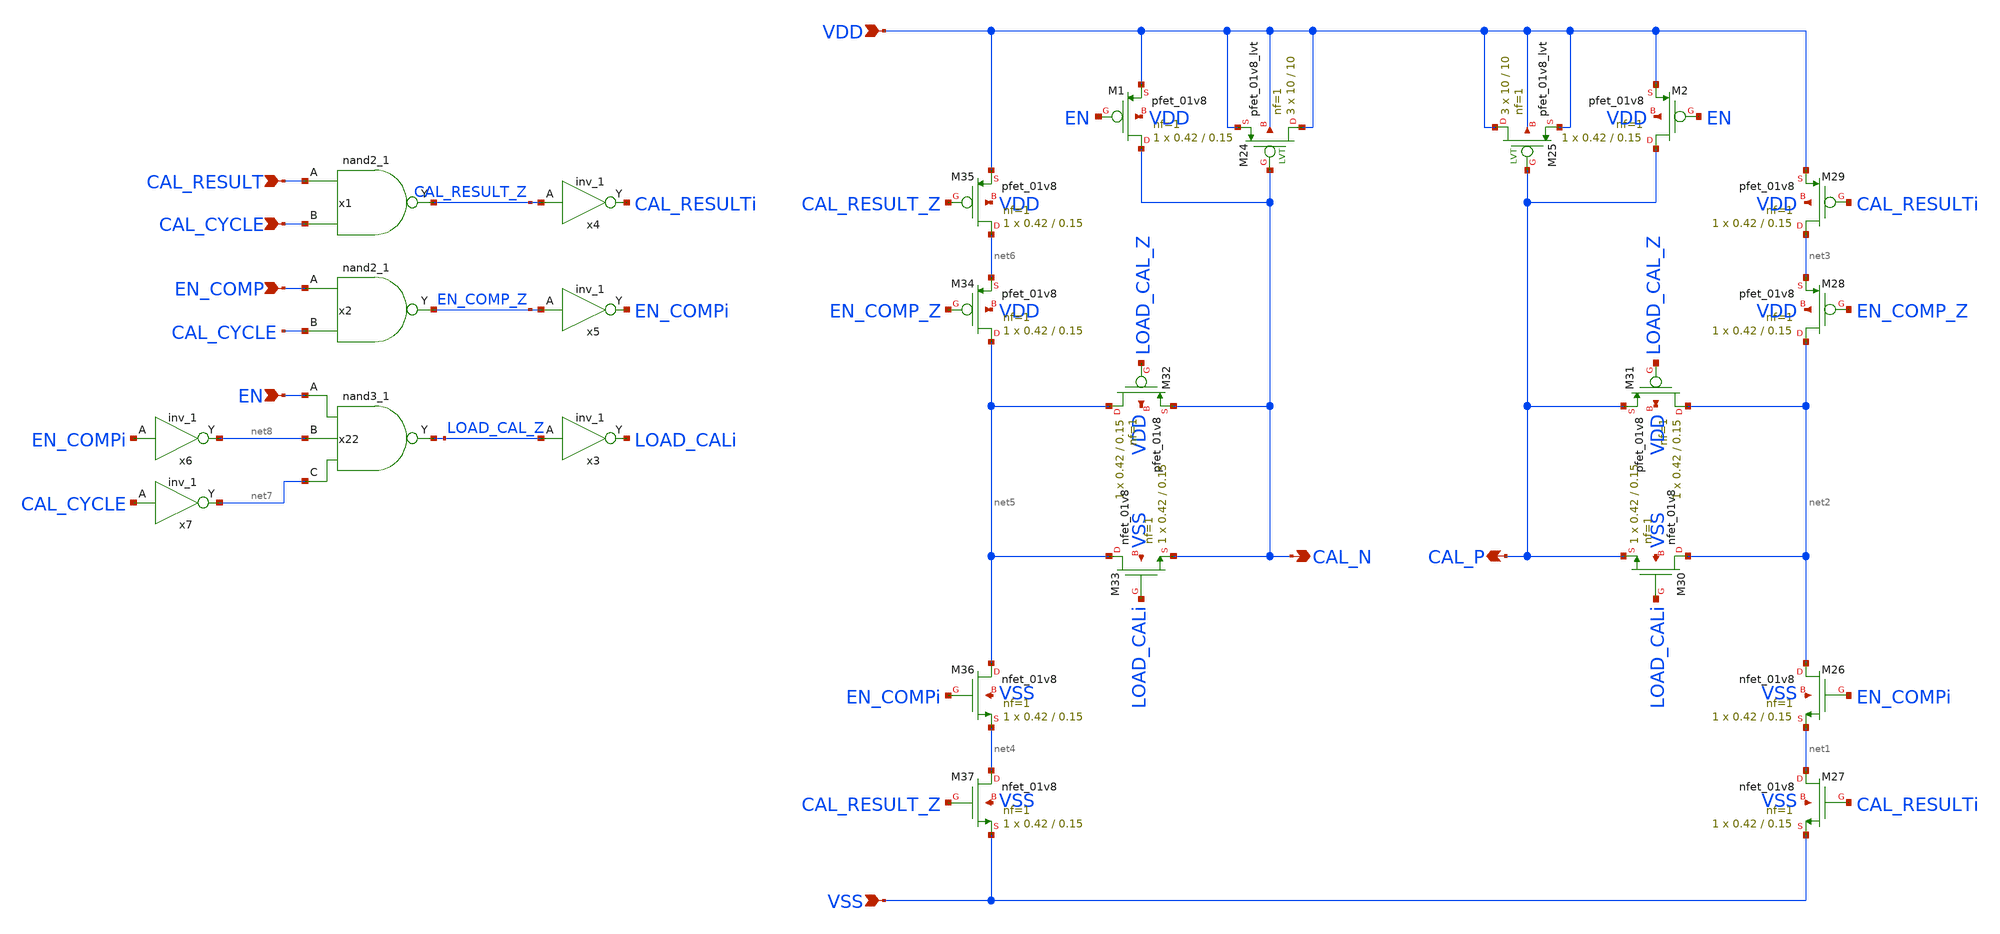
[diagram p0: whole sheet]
** sch_path: offset_calibration/offset_calibration.sch
**.subckt offset_calibration EN_COMP CAL_N CAL_P VDD VSS EN CAL_RESULT CAL_CYCLE
*.ipin EN_COMP
*.opin CAL_N
*.opin CAL_P
*.ipin VDD
*.ipin VSS
*.ipin EN
*.ipin CAL_RESULT
*.ipin CAL_CYCLE
XM26 net2 EN_COMPi net1 VSS sky130_fd_pr__nfet_01v8 L=0.15 W=0.42 nf=1 ad='int((nf+1)/2) * W/nf * 0.29'
+ as='int((nf+2)/2) * W/nf * 0.29' pd='2*int((nf+1)/2) * (W/nf + 0.29)' ps='2*int((nf+2)/2) * (W/nf + 0.29)'
+ nrd='0.29 / W' nrs='0.29 / W' sa=0 sb=0 sd=0 mult=1 m=1
XM27 net1 CAL_RESULTi VSS VSS sky130_fd_pr__nfet_01v8 L=0.15 W=0.42 nf=1 ad='int((nf+1)/2) * W/nf * 0.29'
+ as='int((nf+2)/2) * W/nf * 0.29' pd='2*int((nf+1)/2) * (W/nf + 0.29)' ps='2*int((nf+2)/2) * (W/nf + 0.29)'
+ nrd='0.29 / W' nrs='0.29 / W' sa=0 sb=0 sd=0 mult=1 m=1
XM28 net2 EN_COMP_Z net3 VDD sky130_fd_pr__pfet_01v8 L=0.15 W=0.42 nf=1 ad='int((nf+1)/2) * W/nf * 0.29'
+ as='int((nf+2)/2) * W/nf * 0.29' pd='2*int((nf+1)/2) * (W/nf + 0.29)' ps='2*int((nf+2)/2) * (W/nf + 0.29)'
+ nrd='0.29 / W' nrs='0.29 / W' sa=0 sb=0 sd=0 mult=1 m=1
XM29 net3 CAL_RESULTi VDD VDD sky130_fd_pr__pfet_01v8 L=0.15 W=0.42 nf=1 ad='int((nf+1)/2) * W/nf * 0.29'
+ as='int((nf+2)/2) * W/nf * 0.29' pd='2*int((nf+1)/2) * (W/nf + 0.29)' ps='2*int((nf+2)/2) * (W/nf + 0.29)'
+ nrd='0.29 / W' nrs='0.29 / W' sa=0 sb=0 sd=0 mult=1 m=1
XM30 net2 LOAD_CALi CAL_P VSS sky130_fd_pr__nfet_01v8 L=0.15 W=0.42 nf=1 ad='int((nf+1)/2) * W/nf * 0.29'
+ as='int((nf+2)/2) * W/nf * 0.29' pd='2*int((nf+1)/2) * (W/nf + 0.29)' ps='2*int((nf+2)/2) * (W/nf + 0.29)'
+ nrd='0.29 / W' nrs='0.29 / W' sa=0 sb=0 sd=0 mult=1 m=1
XM31 net2 LOAD_CAL_Z CAL_P VDD sky130_fd_pr__pfet_01v8 L=0.15 W=0.42 nf=1 ad='int((nf+1)/2) * W/nf * 0.29'
+ as='int((nf+2)/2) * W/nf * 0.29' pd='2*int((nf+1)/2) * (W/nf + 0.29)' ps='2*int((nf+2)/2) * (W/nf + 0.29)'
+ nrd='0.29 / W' nrs='0.29 / W' sa=0 sb=0 sd=0 mult=1 m=1
x22 EN net8 net7 VSS VSS VDD VDD LOAD_CAL_Z sky130_fd_sc_hd__nand3_1
x3 LOAD_CAL_Z VSS VSS VDD VDD LOAD_CALi sky130_fd_sc_hd__inv_1
XM32 net5 LOAD_CAL_Z CAL_N VDD sky130_fd_pr__pfet_01v8 L=0.15 W=0.42 nf=1 ad='int((nf+1)/2) * W/nf * 0.29'
+ as='int((nf+2)/2) * W/nf * 0.29' pd='2*int((nf+1)/2) * (W/nf + 0.29)' ps='2*int((nf+2)/2) * (W/nf + 0.29)'
+ nrd='0.29 / W' nrs='0.29 / W' sa=0 sb=0 sd=0 mult=1 m=1
XM33 net5 LOAD_CALi CAL_N VSS sky130_fd_pr__nfet_01v8 L=0.15 W=0.42 nf=1 ad='int((nf+1)/2) * W/nf * 0.29'
+ as='int((nf+2)/2) * W/nf * 0.29' pd='2*int((nf+1)/2) * (W/nf + 0.29)' ps='2*int((nf+2)/2) * (W/nf + 0.29)'
+ nrd='0.29 / W' nrs='0.29 / W' sa=0 sb=0 sd=0 mult=1 m=1
XM34 net5 EN_COMP_Z net6 VDD sky130_fd_pr__pfet_01v8 L=0.15 W=0.42 nf=1 ad='int((nf+1)/2) * W/nf * 0.29'
+ as='int((nf+2)/2) * W/nf * 0.29' pd='2*int((nf+1)/2) * (W/nf + 0.29)' ps='2*int((nf+2)/2) * (W/nf + 0.29)'
+ nrd='0.29 / W' nrs='0.29 / W' sa=0 sb=0 sd=0 mult=1 m=1
XM35 net6 CAL_RESULT_Z VDD VDD sky130_fd_pr__pfet_01v8 L=0.15 W=0.42 nf=1 ad='int((nf+1)/2) * W/nf * 0.29'
+ as='int((nf+2)/2) * W/nf * 0.29' pd='2*int((nf+1)/2) * (W/nf + 0.29)' ps='2*int((nf+2)/2) * (W/nf + 0.29)'
+ nrd='0.29 / W' nrs='0.29 / W' sa=0 sb=0 sd=0 mult=1 m=1
XM36 net5 EN_COMPi net4 VSS sky130_fd_pr__nfet_01v8 L=0.15 W=0.42 nf=1 ad='int((nf+1)/2) * W/nf * 0.29'
+ as='int((nf+2)/2) * W/nf * 0.29' pd='2*int((nf+1)/2) * (W/nf + 0.29)' ps='2*int((nf+2)/2) * (W/nf + 0.29)'
+ nrd='0.29 / W' nrs='0.29 / W' sa=0 sb=0 sd=0 mult=1 m=1
XM37 net4 CAL_RESULT_Z VSS VSS sky130_fd_pr__nfet_01v8 L=0.15 W=0.42 nf=1 ad='int((nf+1)/2) * W/nf * 0.29'
+ as='int((nf+2)/2) * W/nf * 0.29' pd='2*int((nf+1)/2) * (W/nf + 0.29)' ps='2*int((nf+2)/2) * (W/nf + 0.29)'
+ nrd='0.29 / W' nrs='0.29 / W' sa=0 sb=0 sd=0 mult=1 m=1
XM24 VDD CAL_N VDD VDD sky130_fd_pr__pfet_01v8_lvt L=10 W=10 nf=1 ad='int((nf+1)/2) * W/nf * 0.29' as='int((nf+2)/2) * W/nf * 0.29'
+ pd='2*int((nf+1)/2) * (W/nf + 0.29)' ps='2*int((nf+2)/2) * (W/nf + 0.29)' nrd='0.29 / W' nrs='0.29 / W'
+ sa=0 sb=0 sd=0 mult=3 m=3
XM25 VDD CAL_P VDD VDD sky130_fd_pr__pfet_01v8_lvt L=10 W=10 nf=1 ad='int((nf+1)/2) * W/nf * 0.29' as='int((nf+2)/2) * W/nf * 0.29'
+ pd='2*int((nf+1)/2) * (W/nf + 0.29)' ps='2*int((nf+2)/2) * (W/nf + 0.29)' nrd='0.29 / W' nrs='0.29 / W'
+ sa=0 sb=0 sd=0 mult=3 m=3
XM1 CAL_N EN VDD VDD sky130_fd_pr__pfet_01v8 L=0.15 W=0.42 nf=1 ad='int((nf+1)/2) * W/nf * 0.29' as='int((nf+2)/2) * W/nf * 0.29'
+ pd='2*int((nf+1)/2) * (W/nf + 0.29)' ps='2*int((nf+2)/2) * (W/nf + 0.29)' nrd='0.29 / W' nrs='0.29 / W'
+ sa=0 sb=0 sd=0 mult=1 m=1
XM2 CAL_P EN VDD VDD sky130_fd_pr__pfet_01v8 L=0.15 W=0.42 nf=1 ad='int((nf+1)/2) * W/nf * 0.29' as='int((nf+2)/2) * W/nf * 0.29'
+ pd='2*int((nf+1)/2) * (W/nf + 0.29)' ps='2*int((nf+2)/2) * (W/nf + 0.29)' nrd='0.29 / W' nrs='0.29 / W'
+ sa=0 sb=0 sd=0 mult=1 m=1
x1 CAL_RESULT CAL_CYCLE VSS VSS VDD VDD CAL_RESULT_Z sky130_fd_sc_hd__nand2_1
x4 CAL_RESULT_Z VSS VSS VDD VDD CAL_RESULTi sky130_fd_sc_hd__inv_1
x2 EN_COMP CAL_CYCLE VSS VSS VDD VDD EN_COMP_Z sky130_fd_sc_hd__nand2_1
x5 EN_COMP_Z VSS VSS VDD VDD EN_COMPi sky130_fd_sc_hd__inv_1
x6 EN_COMPi VSS VSS VDD VDD net8 sky130_fd_sc_hd__inv_1
x7 CAL_CYCLE VSS VSS VDD VDD net7 sky130_fd_sc_hd__inv_1
**.ends
.end
